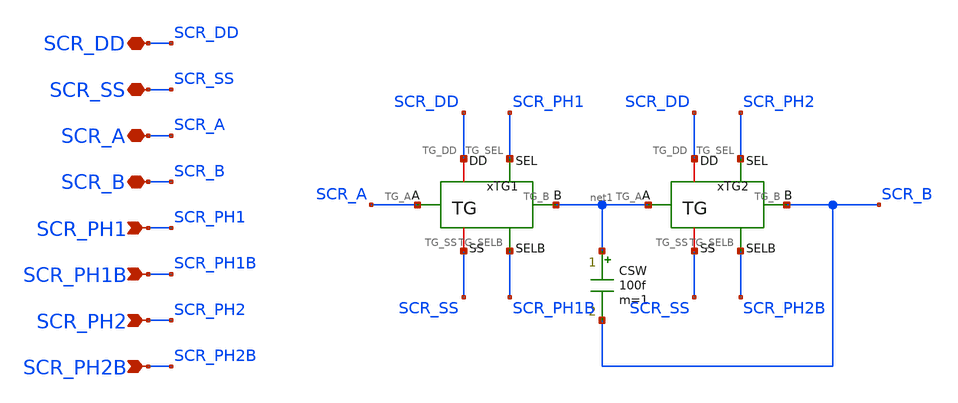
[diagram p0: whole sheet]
** sch_path: Design_Files/IC Design/Schematic/SCR/SCR.sch
**.subckt SCR SCR_DD SCR_SS SCR_PH1 SCR_A SCR_B SCR_PH1B SCR_PH2 SCR_PH2B
*.iopin SCR_DD
*.iopin SCR_SS
*.ipin SCR_PH1
*.iopin SCR_A
*.iopin SCR_B
*.ipin SCR_PH1B
*.ipin SCR_PH2
*.ipin SCR_PH2B
CSW net1 SCR_B 100f m=1
xTG1 SCR_DD SCR_SS SCR_A net1 SCR_PH1 SCR_PH1B TG
xTG2 SCR_DD SCR_SS net1 SCR_B SCR_PH2 SCR_PH2B TG
**.ends

* expanding   symbol:  ECG_Acquisition_IC/Design_Files/IC Design/Schematic/TG/TG.sym # of pins=6
** sym_path: Design_Files/IC Design/Schematic/TG/TG.sym
** sch_path: Design_Files/IC Design/Schematic/TG/TG.sch
.subckt TG TG_DD TG_SS TG_A TG_B TG_SEL TG_SELB
*.iopin TG_DD
*.iopin TG_SS
*.iopin TG_A
*.iopin TG_B
*.ipin TG_SEL
*.ipin TG_SELB
XMTGP TG_B TG_SELB TG_A TG_DD pfet_03v3 L=0.5u W=10u nf=1 ad='int((nf+1)/2) * W/nf * 0.18u' as='int((nf+2)/2) * W/nf * 0.18u'
+ pd='2*int((nf+1)/2) * (W/nf + 0.18u)' ps='2*int((nf+2)/2) * (W/nf + 0.18u)' nrd='0.18u / W' nrs='0.18u / W'
+ sa=0 sb=0 sd=0 m=1
XMTGN TG_A TG_SEL TG_B TG_SS nfet_03v3 L=0.5u W=5u nf=1 ad='int((nf+1)/2) * W/nf * 0.18u' as='int((nf+2)/2) * W/nf * 0.18u'
+ pd='2*int((nf+1)/2) * (W/nf + 0.18u)' ps='2*int((nf+2)/2) * (W/nf + 0.18u)' nrd='0.18u / W' nrs='0.18u / W'
+ sa=0 sb=0 sd=0 m=1
.ends

.end
